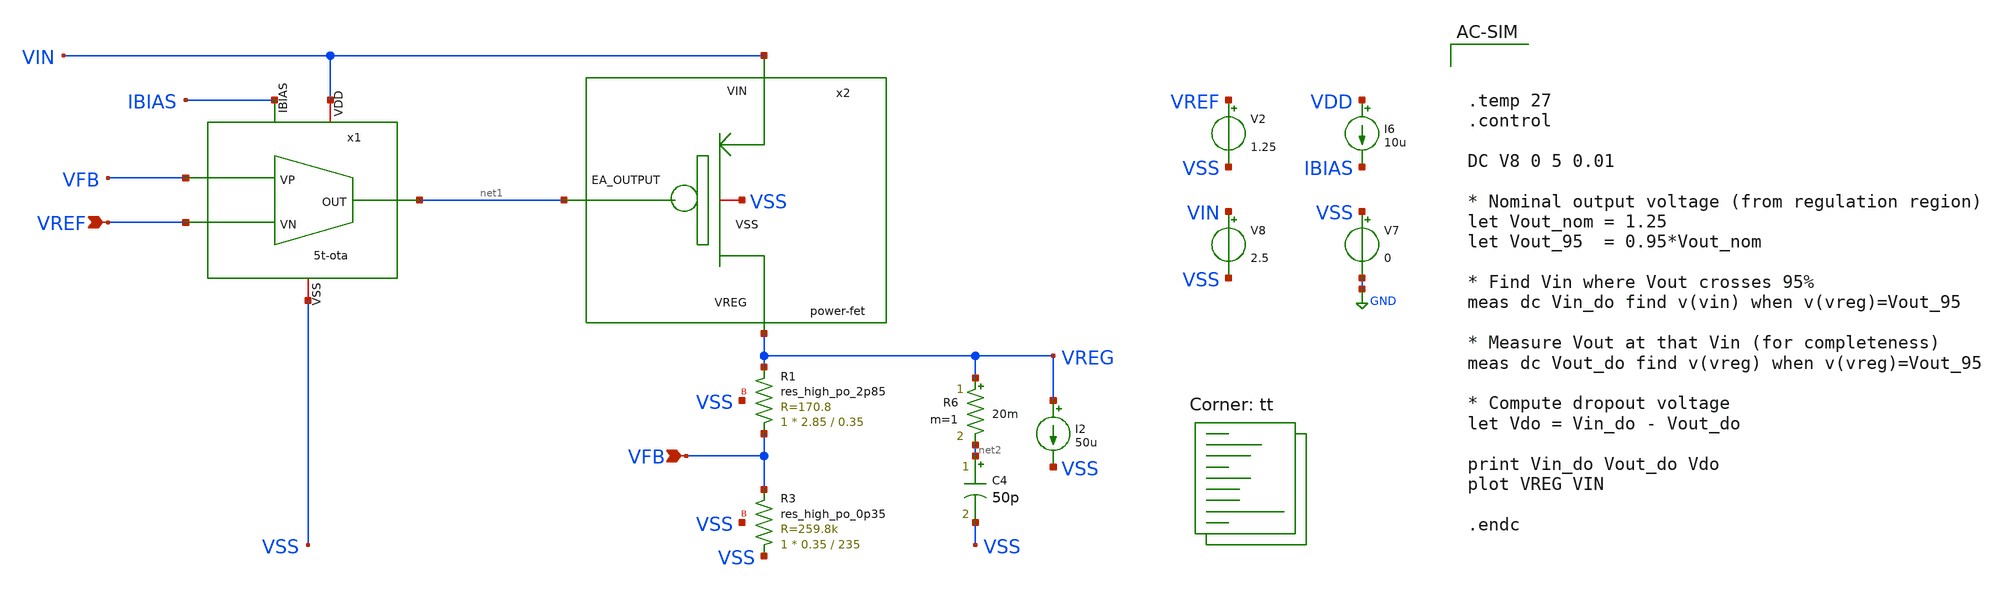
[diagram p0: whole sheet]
** sch_path: xschem/ldo-core/schematics/ldo-ota-only.sch
**.subckt ldo-ota-only VFB VREF
*.ipin VFB
*.ipin VREF
x1 VIN net1 IBIAS VREF VFB VSS 5t-ota
x2 VIN VSS net1 VREG power-fet
XR3 VSS VFB VSS sky130_fd_pr__res_high_po_0p35 L=235 mult=1 m=1
XR1 VFB VREG VSS sky130_fd_pr__res_high_po_2p85 L=0.35 mult=1 m=1
V2 VREF VSS 1.25
I6 VDD IBIAS 10u
V7 VSS GND 0
V8 VIN VSS 2.5
I2 VREG VSS 50u
C4 net2 VSS 50p m=1
R6 VREG net2 20m m=1
**** begin user architecture code



.temp 27
.control

DC V8 0 5 0.01

* Nominal output voltage (from regulation region)
let Vout_nom = 1.25
let Vout_95  = 0.95*Vout_nom

* Find Vin where Vout crosses 95%
meas dc Vin_do find v(vin) when v(vreg)=Vout_95

* Measure Vout at that Vin (for completeness)
meas dc Vout_do find v(vreg) when v(vreg)=Vout_95

* Compute dropout voltage
let Vdo = Vin_do - Vout_do

print Vin_do Vout_do Vdo
plot VREG VIN

.endc


.lib $::SKYWATER_MODELS/sky130.lib.spice tt
**** end user architecture code
**.ends
.GLOBAL GND
.end
